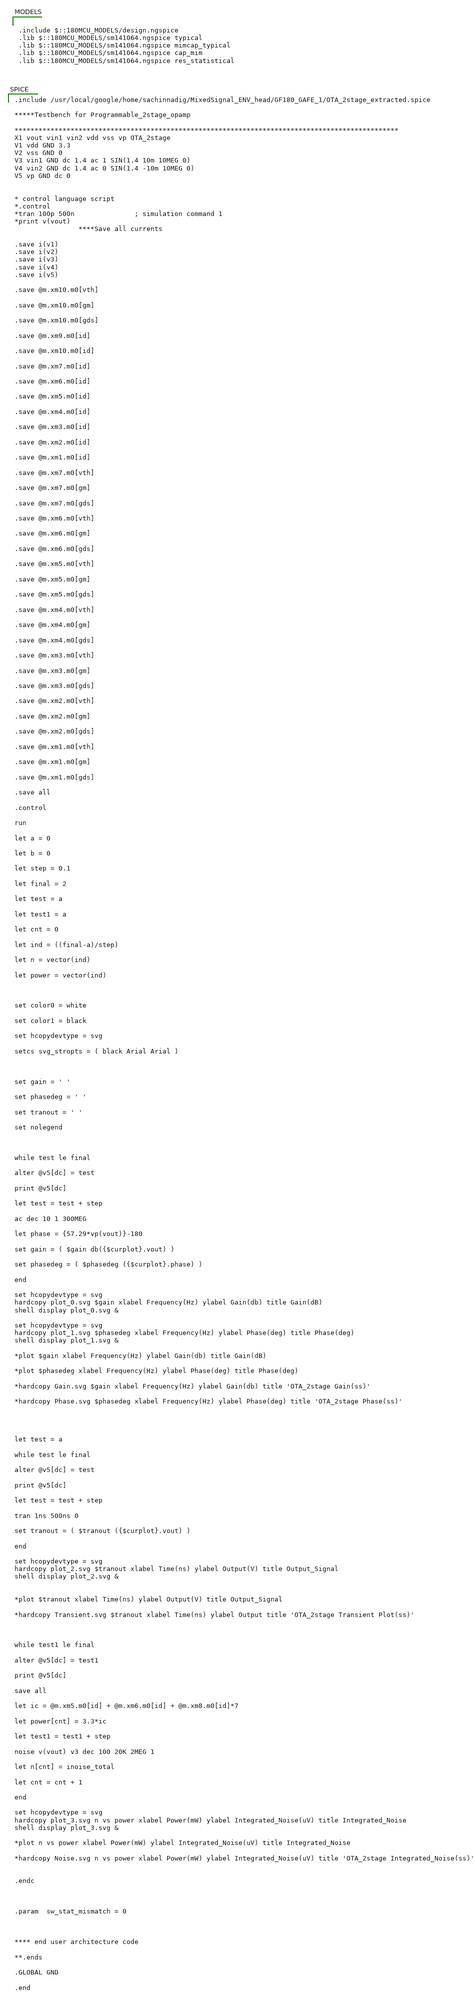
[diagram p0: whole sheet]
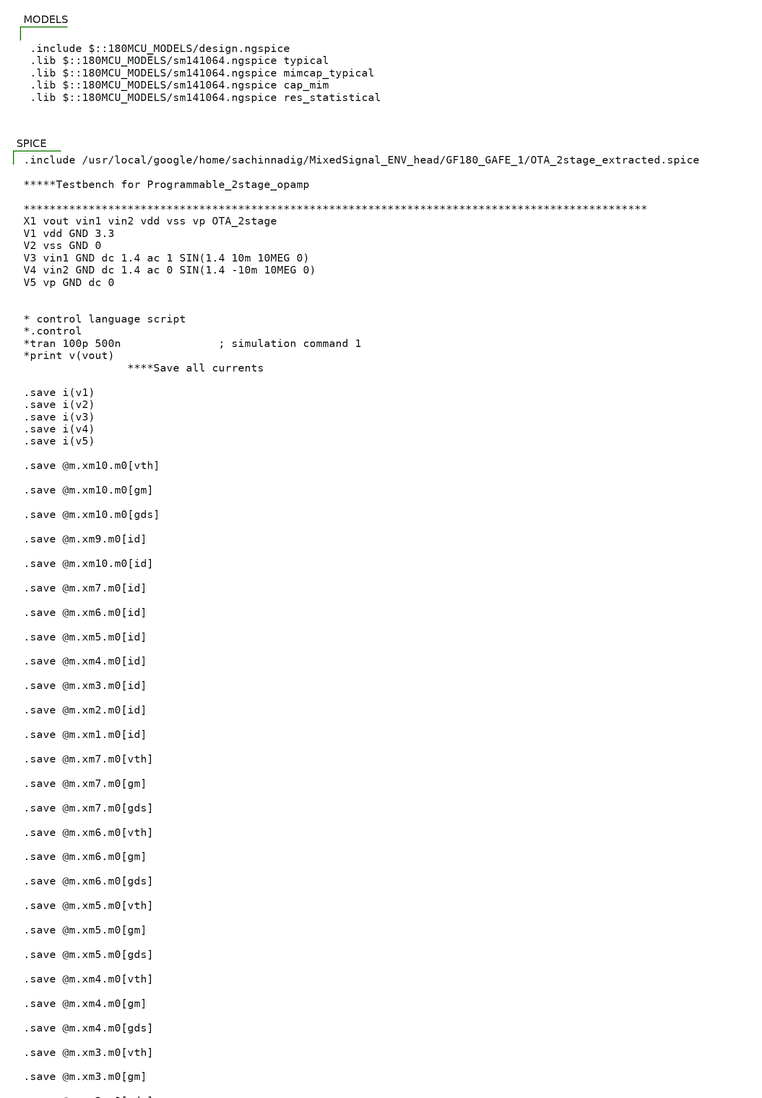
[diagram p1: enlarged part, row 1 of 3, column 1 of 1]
** sch_path: Programmable_2stage_opamp_TB.sch
**.subckt Programmable_2stage_opamp_TB
**** begin user architecture code

.include $::180MCU_MODELS/design.ngspice
.lib $::180MCU_MODELS/sm141064.ngspice typical
.lib $::180MCU_MODELS/sm141064.ngspice mimcap_typical
.lib $::180MCU_MODELS/sm141064.ngspice cap_mim
.lib $::180MCU_MODELS/sm141064.ngspice res_statistical


.include /usr/local/google/home/sachinnadig/MixedSignal_ENV_head/GF180_GAFE_1/OTA_2stage_extracted.spice

*****Testbench for Programmable_2stage_opamp

************************************************************************************************
X1 vout vin1 vin2 vdd vss vp OTA_2stage
V1 vdd GND 3.3
V2 vss GND 0
V3 vin1 GND dc 1.4 ac 1 SIN(1.4 10m 10MEG 0)
V4 vin2 GND dc 1.4 ac 0 SIN(1.4 -10m 10MEG 0)
V5 vp GND dc 0


* control language script
*.control
*tran 100p 500n               ; simulation command 1
*print v(vout)
                ****Save all currents

.save i(v1)
.save i(v2)
.save i(v3)
.save i(v4)
.save i(v5)

.save @m.xm10.m0[vth]

.save @m.xm10.m0[gm]

.save @m.xm10.m0[gds]

.save @m.xm9.m0[id]

.save @m.xm10.m0[id]

.save @m.xm7.m0[id]

.save @m.xm6.m0[id]

.save @m.xm5.m0[id]

.save @m.xm4.m0[id]

.save @m.xm3.m0[id]

.save @m.xm2.m0[id]

.save @m.xm1.m0[id]

.save @m.xm7.m0[vth]

.save @m.xm7.m0[gm]

.save @m.xm7.m0[gds]

.save @m.xm6.m0[vth]

.save @m.xm6.m0[gm]

.save @m.xm6.m0[gds]

.save @m.xm5.m0[vth]

.save @m.xm5.m0[gm]

.save @m.xm5.m0[gds]

.save @m.xm4.m0[vth]

.save @m.xm4.m0[gm]

.save @m.xm4.m0[gds]

.save @m.xm3.m0[vth]

.save @m.xm3.m0[gm]

.save @m.xm3.m0[gds]

.save @m.xm2.m0[vth]

.save @m.xm2.m0[gm]

.save @m.xm2.m0[gds]

.save @m.xm1.m0[vth]

.save @m.xm1.m0[gm]

.save @m.xm1.m0[gds]

.save all

.control

run

let a = 0

let b = 0

let step = 0.1

let final = 2

let test = a

let test1 = a

let cnt = 0

let ind = ((final-a)/step)

let n = vector(ind)

let power = vector(ind)



set color0 = white

set color1 = black

set hcopydevtype = svg

setcs svg_stropts = ( black Arial Arial )



set gain = ' '

set phasedeg = ' '

set tranout = ' '

set nolegend



while test le final

alter @v5[dc] = test

print @v5[dc]

let test = test + step

ac dec 10 1 300MEG

let phase = {57.29*vp(vout)}-180

set gain = ( $gain db({$curplot}.vout) )

set phasedeg = ( $phasedeg ({$curplot}.phase) )

end

set hcopydevtype = svg
hardcopy plot_0.svg $gain xlabel Frequency(Hz) ylabel Gain(db) title Gain(dB)
shell display plot_0.svg &

set hcopydevtype = svg
hardcopy plot_1.svg $phasedeg xlabel Frequency(Hz) ylabel Phase(deg) title Phase(deg)
shell display plot_1.svg &

*plot $gain xlabel Frequency(Hz) ylabel Gain(db) title Gain(dB)

*plot $phasedeg xlabel Frequency(Hz) ylabel Phase(deg) title Phase(deg)

*hardcopy Gain.svg $gain xlabel Frequency(Hz) ylabel Gain(db) title 'OTA_2stage Gain(ss)'

*hardcopy Phase.svg $phasedeg xlabel Frequency(Hz) ylabel Phase(deg) title 'OTA_2stage Phase(ss)'




let test = a

while test le final

alter @v5[dc] = test

print @v5[dc]

let test = test + step

tran 1ns 500ns 0

set tranout = ( $tranout ({$curplot}.vout) )

end

set hcopydevtype = svg
hardcopy plot_2.svg $tranout xlabel Time(ns) ylabel Output(V) title Output_Signal
shell display plot_2.svg &


*plot $tranout xlabel Time(ns) ylabel Output(V) title Output_Signal

*hardcopy Transient.svg $tranout xlabel Time(ns) ylabel Output title 'OTA_2stage Transient Plot(ss)'



while test1 le final

alter @v5[dc] = test1

print @v5[dc]

save all

let ic = @m.xm5.m0[id] + @m.xm6.m0[id] + @m.xm8.m0[id]*7

let power[cnt] = 3.3*ic

let test1 = test1 + step

noise v(vout) v3 dec 100 20K 2MEG 1

let n[cnt] = inoise_total

let cnt = cnt + 1

end

set hcopydevtype = svg
hardcopy plot_3.svg n vs power xlabel Power(mW) ylabel Integrated_Noise(uV) title Integrated_Noise
shell display plot_3.svg &

*plot n vs power xlabel Power(mW) ylabel Integrated_Noise(uV) title Integrated_Noise

*hardcopy Noise.svg n vs power xlabel Power(mW) ylabel Integrated_Noise(uV) title 'OTA_2stage Integrated_Noise(ss)'


.endc



.param  sw_stat_mismatch = 0



**** end user architecture code

**.ends

.GLOBAL GND

.end



**** end user architecture code
**.ends
.end
